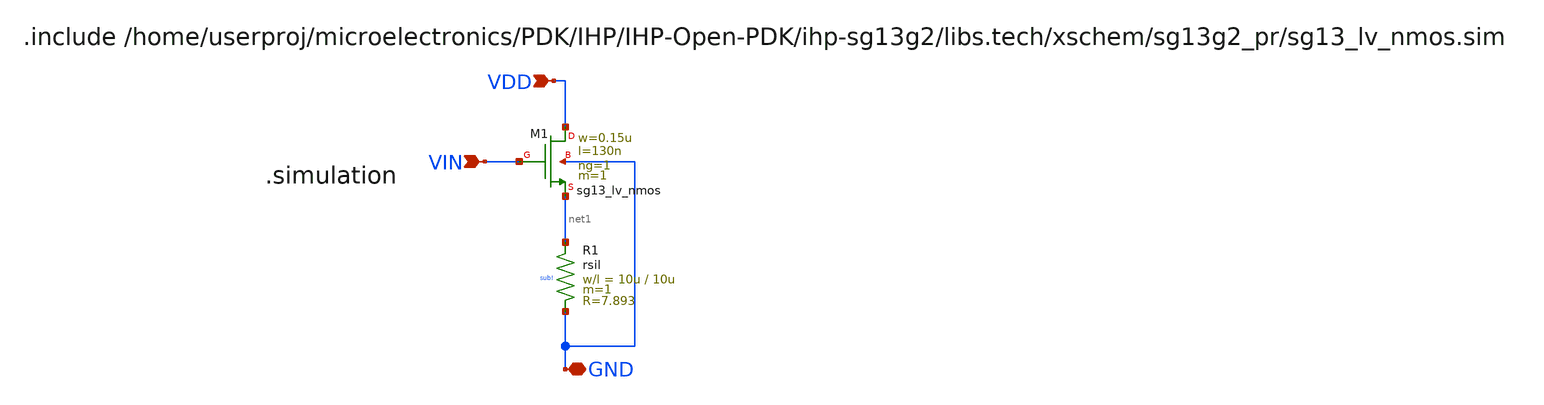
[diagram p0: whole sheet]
** sch_path: LVS/xschem/BGM_AA/NMOS_RESISTANCE/TOP.sch
**.subckt TOP VIN GND VDD
*.ipin VIN
*.iopin GND
*.ipin VDD
XM1 VDD VIN net1 GND sg13_lv_nmos w=0.15u l=130n ng=1 m=1 mm_ok=1
XR1 net1 GND sub! rsil w=10u l=10u m=1 mm_ok=1
**.ends
.end
